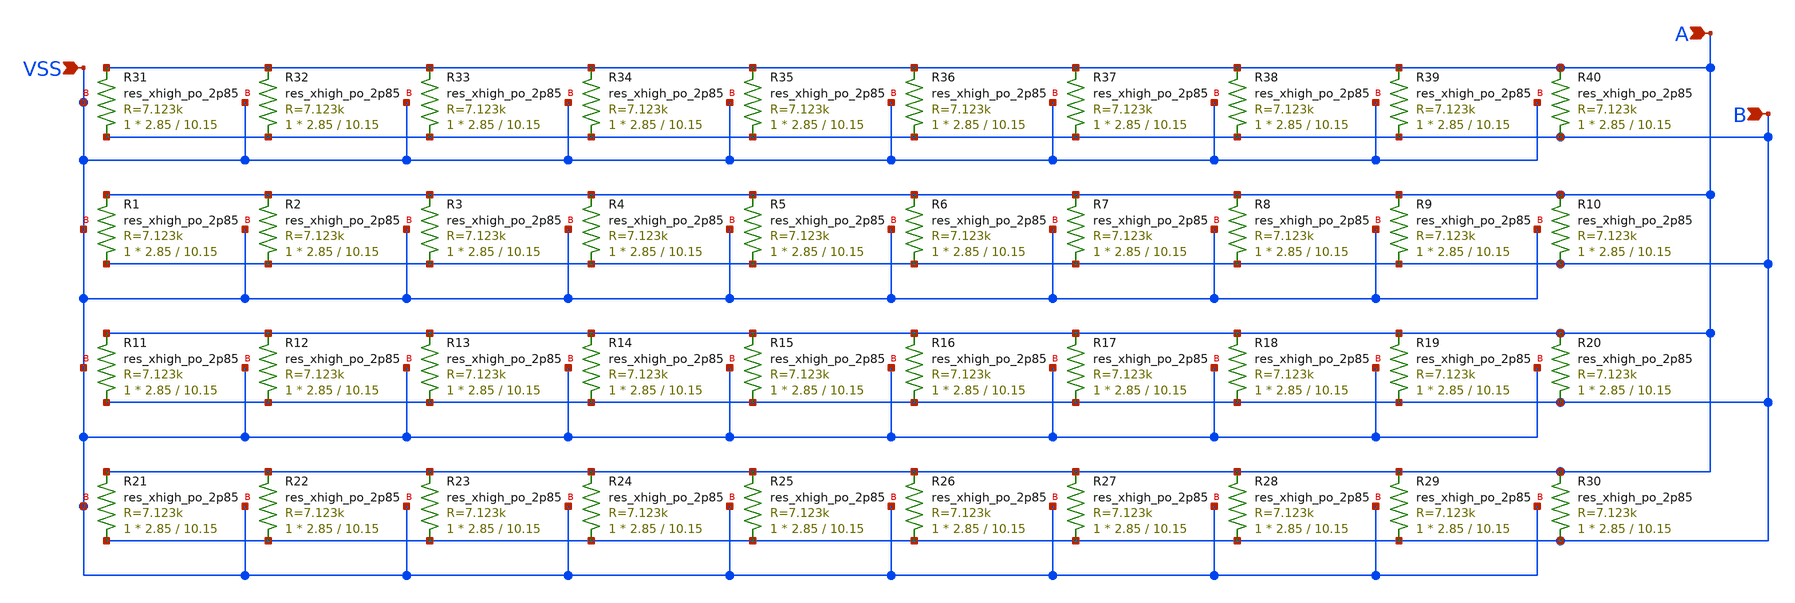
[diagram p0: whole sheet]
** sch_path: integrasi/integrasi/resistor_paralel/resistor180.sch
**.subckt resistor180 A B VSS
*.ipin A
*.ipin B
*.ipin VSS
XR1 B A VSS sky130_fd_pr__res_xhigh_po_2p85 L=10.15 mult=1 m=1
XR2 B A VSS sky130_fd_pr__res_xhigh_po_2p85 L=10.15 mult=1 m=1
XR3 B A VSS sky130_fd_pr__res_xhigh_po_2p85 L=10.15 mult=1 m=1
XR4 B A VSS sky130_fd_pr__res_xhigh_po_2p85 L=10.15 mult=1 m=1
XR5 B A VSS sky130_fd_pr__res_xhigh_po_2p85 L=10.15 mult=1 m=1
XR6 B A VSS sky130_fd_pr__res_xhigh_po_2p85 L=10.15 mult=1 m=1
XR7 B A VSS sky130_fd_pr__res_xhigh_po_2p85 L=10.15 mult=1 m=1
XR8 B A VSS sky130_fd_pr__res_xhigh_po_2p85 L=10.15 mult=1 m=1
XR9 B A VSS sky130_fd_pr__res_xhigh_po_2p85 L=10.15 mult=1 m=1
XR10 B A VSS sky130_fd_pr__res_xhigh_po_2p85 L=10.15 mult=1 m=1
XR11 B A VSS sky130_fd_pr__res_xhigh_po_2p85 L=10.15 mult=1 m=1
XR12 B A VSS sky130_fd_pr__res_xhigh_po_2p85 L=10.15 mult=1 m=1
XR13 B A VSS sky130_fd_pr__res_xhigh_po_2p85 L=10.15 mult=1 m=1
XR14 B A VSS sky130_fd_pr__res_xhigh_po_2p85 L=10.15 mult=1 m=1
XR15 B A VSS sky130_fd_pr__res_xhigh_po_2p85 L=10.15 mult=1 m=1
XR16 B A VSS sky130_fd_pr__res_xhigh_po_2p85 L=10.15 mult=1 m=1
XR17 B A VSS sky130_fd_pr__res_xhigh_po_2p85 L=10.15 mult=1 m=1
XR18 B A VSS sky130_fd_pr__res_xhigh_po_2p85 L=10.15 mult=1 m=1
XR19 B A VSS sky130_fd_pr__res_xhigh_po_2p85 L=10.15 mult=1 m=1
XR20 B A VSS sky130_fd_pr__res_xhigh_po_2p85 L=10.15 mult=1 m=1
XR21 B A VSS sky130_fd_pr__res_xhigh_po_2p85 L=10.15 mult=1 m=1
XR22 B A VSS sky130_fd_pr__res_xhigh_po_2p85 L=10.15 mult=1 m=1
XR23 B A VSS sky130_fd_pr__res_xhigh_po_2p85 L=10.15 mult=1 m=1
XR24 B A VSS sky130_fd_pr__res_xhigh_po_2p85 L=10.15 mult=1 m=1
XR25 B A VSS sky130_fd_pr__res_xhigh_po_2p85 L=10.15 mult=1 m=1
XR26 B A VSS sky130_fd_pr__res_xhigh_po_2p85 L=10.15 mult=1 m=1
XR27 B A VSS sky130_fd_pr__res_xhigh_po_2p85 L=10.15 mult=1 m=1
XR28 B A VSS sky130_fd_pr__res_xhigh_po_2p85 L=10.15 mult=1 m=1
XR29 B A VSS sky130_fd_pr__res_xhigh_po_2p85 L=10.15 mult=1 m=1
XR30 B A VSS sky130_fd_pr__res_xhigh_po_2p85 L=10.15 mult=1 m=1
XR31 B A VSS sky130_fd_pr__res_xhigh_po_2p85 L=10.15 mult=1 m=1
XR32 B A VSS sky130_fd_pr__res_xhigh_po_2p85 L=10.15 mult=1 m=1
XR33 B A VSS sky130_fd_pr__res_xhigh_po_2p85 L=10.15 mult=1 m=1
XR34 B A VSS sky130_fd_pr__res_xhigh_po_2p85 L=10.15 mult=1 m=1
XR35 B A VSS sky130_fd_pr__res_xhigh_po_2p85 L=10.15 mult=1 m=1
XR36 B A VSS sky130_fd_pr__res_xhigh_po_2p85 L=10.15 mult=1 m=1
XR37 B A VSS sky130_fd_pr__res_xhigh_po_2p85 L=10.15 mult=1 m=1
XR38 B A VSS sky130_fd_pr__res_xhigh_po_2p85 L=10.15 mult=1 m=1
XR39 B A VSS sky130_fd_pr__res_xhigh_po_2p85 L=10.15 mult=1 m=1
XR40 B A VSS sky130_fd_pr__res_xhigh_po_2p85 L=10.15 mult=1 m=1
**.ends
.end
